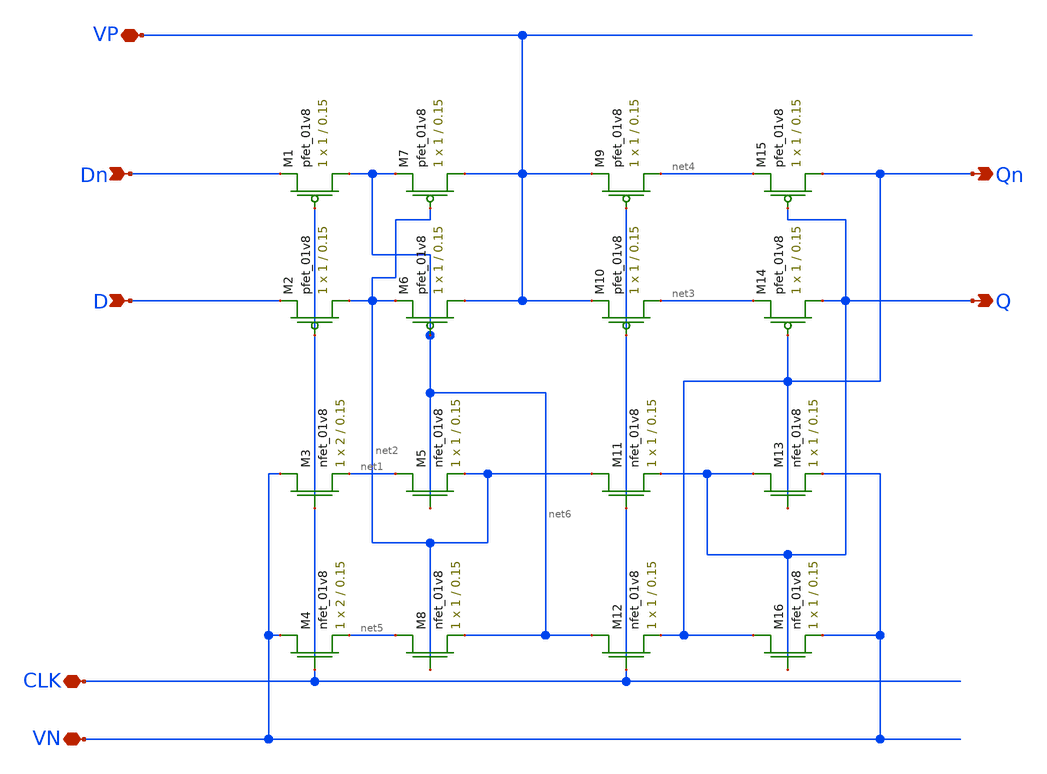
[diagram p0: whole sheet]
** sch_path: MP2/csrl.sch
**.subckt csrl VP VN CLK Dn D Qn Q
*.iopin VP
*.iopin VN
*.iopin CLK
*.ipin Dn
*.ipin D
*.opin Qn
*.opin Q
XM1 net6 CLK Dn VDD sky130_fd_pr__pfet_01v8 L=0.15 W=1 nf=1 ad='int((nf+1)/2) * W/nf * 0.29' as='int((nf+2)/2) * W/nf * 0.29'
+ pd='2*int((nf+1)/2) * (W/nf + 0.29)' ps='2*int((nf+2)/2) * (W/nf + 0.29)' nrd='0.29 / W' nrs='0.29 / W'
+ sa=0 sb=0 sd=0 mult=1 m=1
XM2 net2 CLK D VDD sky130_fd_pr__pfet_01v8 L=0.15 W=1 nf=1 ad='int((nf+1)/2) * W/nf * 0.29' as='int((nf+2)/2) * W/nf * 0.29'
+ pd='2*int((nf+1)/2) * (W/nf + 0.29)' ps='2*int((nf+2)/2) * (W/nf + 0.29)' nrd='0.29 / W' nrs='0.29 / W'
+ sa=0 sb=0 sd=0 mult=1 m=1
XM3 VN CLK net1 GND sky130_fd_pr__nfet_01v8 L=0.15 W=2 nf=1 ad='int((nf+1)/2) * W/nf * 0.29' as='int((nf+2)/2) * W/nf * 0.29'
+ pd='2*int((nf+1)/2) * (W/nf + 0.29)' ps='2*int((nf+2)/2) * (W/nf + 0.29)' nrd='0.29 / W' nrs='0.29 / W'
+ sa=0 sb=0 sd=0 mult=1 m=1
XM4 VN CLK net5 GND sky130_fd_pr__nfet_01v8 L=0.15 W=2 nf=1 ad='int((nf+1)/2) * W/nf * 0.29' as='int((nf+2)/2) * W/nf * 0.29'
+ pd='2*int((nf+1)/2) * (W/nf + 0.29)' ps='2*int((nf+2)/2) * (W/nf + 0.29)' nrd='0.29 / W' nrs='0.29 / W'
+ sa=0 sb=0 sd=0 mult=1 m=1
XM5 net1 net6 net2 GND sky130_fd_pr__nfet_01v8 L=0.15 W=1 nf=1 ad='int((nf+1)/2) * W/nf * 0.29' as='int((nf+2)/2) * W/nf * 0.29'
+ pd='2*int((nf+1)/2) * (W/nf + 0.29)' ps='2*int((nf+2)/2) * (W/nf + 0.29)' nrd='0.29 / W' nrs='0.29 / W'
+ sa=0 sb=0 sd=0 mult=1 m=1
XM6 VP net6 net2 VDD sky130_fd_pr__pfet_01v8 L=0.15 W=1 nf=1 ad='int((nf+1)/2) * W/nf * 0.29' as='int((nf+2)/2) * W/nf * 0.29'
+ pd='2*int((nf+1)/2) * (W/nf + 0.29)' ps='2*int((nf+2)/2) * (W/nf + 0.29)' nrd='0.29 / W' nrs='0.29 / W'
+ sa=0 sb=0 sd=0 mult=1 m=1
XM7 VP net2 net6 VDD sky130_fd_pr__pfet_01v8 L=0.15 W=1 nf=1 ad='int((nf+1)/2) * W/nf * 0.29' as='int((nf+2)/2) * W/nf * 0.29'
+ pd='2*int((nf+1)/2) * (W/nf + 0.29)' ps='2*int((nf+2)/2) * (W/nf + 0.29)' nrd='0.29 / W' nrs='0.29 / W'
+ sa=0 sb=0 sd=0 mult=1 m=1
XM8 net5 net2 net6 GND sky130_fd_pr__nfet_01v8 L=0.15 W=1 nf=1 ad='int((nf+1)/2) * W/nf * 0.29' as='int((nf+2)/2) * W/nf * 0.29'
+ pd='2*int((nf+1)/2) * (W/nf + 0.29)' ps='2*int((nf+2)/2) * (W/nf + 0.29)' nrd='0.29 / W' nrs='0.29 / W'
+ sa=0 sb=0 sd=0 mult=1 m=1
XM9 net4 CLK VP VDD sky130_fd_pr__pfet_01v8 L=0.15 W=1 nf=1 ad='int((nf+1)/2) * W/nf * 0.29' as='int((nf+2)/2) * W/nf * 0.29'
+ pd='2*int((nf+1)/2) * (W/nf + 0.29)' ps='2*int((nf+2)/2) * (W/nf + 0.29)' nrd='0.29 / W' nrs='0.29 / W'
+ sa=0 sb=0 sd=0 mult=1 m=1
XM10 net3 CLK VP VDD sky130_fd_pr__pfet_01v8 L=0.15 W=1 nf=1 ad='int((nf+1)/2) * W/nf * 0.29' as='int((nf+2)/2) * W/nf * 0.29'
+ pd='2*int((nf+1)/2) * (W/nf + 0.29)' ps='2*int((nf+2)/2) * (W/nf + 0.29)' nrd='0.29 / W' nrs='0.29 / W'
+ sa=0 sb=0 sd=0 mult=1 m=1
XM11 net2 CLK Q GND sky130_fd_pr__nfet_01v8 L=0.15 W=1 nf=1 ad='int((nf+1)/2) * W/nf * 0.29' as='int((nf+2)/2) * W/nf * 0.29'
+ pd='2*int((nf+1)/2) * (W/nf + 0.29)' ps='2*int((nf+2)/2) * (W/nf + 0.29)' nrd='0.29 / W' nrs='0.29 / W'
+ sa=0 sb=0 sd=0 mult=1 m=1
XM12 net6 CLK Qn GND sky130_fd_pr__nfet_01v8 L=0.15 W=1 nf=1 ad='int((nf+1)/2) * W/nf * 0.29' as='int((nf+2)/2) * W/nf * 0.29'
+ pd='2*int((nf+1)/2) * (W/nf + 0.29)' ps='2*int((nf+2)/2) * (W/nf + 0.29)' nrd='0.29 / W' nrs='0.29 / W'
+ sa=0 sb=0 sd=0 mult=1 m=1
XM13 Q Qn VN GND sky130_fd_pr__nfet_01v8 L=0.15 W=1 nf=1 ad='int((nf+1)/2) * W/nf * 0.29' as='int((nf+2)/2) * W/nf * 0.29'
+ pd='2*int((nf+1)/2) * (W/nf + 0.29)' ps='2*int((nf+2)/2) * (W/nf + 0.29)' nrd='0.29 / W' nrs='0.29 / W'
+ sa=0 sb=0 sd=0 mult=1 m=1
XM14 Q Qn net3 VDD sky130_fd_pr__pfet_01v8 L=0.15 W=1 nf=1 ad='int((nf+1)/2) * W/nf * 0.29' as='int((nf+2)/2) * W/nf * 0.29'
+ pd='2*int((nf+1)/2) * (W/nf + 0.29)' ps='2*int((nf+2)/2) * (W/nf + 0.29)' nrd='0.29 / W' nrs='0.29 / W'
+ sa=0 sb=0 sd=0 mult=1 m=1
XM15 Qn Q net4 VDD sky130_fd_pr__pfet_01v8 L=0.15 W=1 nf=1 ad='int((nf+1)/2) * W/nf * 0.29' as='int((nf+2)/2) * W/nf * 0.29'
+ pd='2*int((nf+1)/2) * (W/nf + 0.29)' ps='2*int((nf+2)/2) * (W/nf + 0.29)' nrd='0.29 / W' nrs='0.29 / W'
+ sa=0 sb=0 sd=0 mult=1 m=1
XM16 Qn Q VN GND sky130_fd_pr__nfet_01v8 L=0.15 W=1 nf=1 ad='int((nf+1)/2) * W/nf * 0.29' as='int((nf+2)/2) * W/nf * 0.29'
+ pd='2*int((nf+1)/2) * (W/nf + 0.29)' ps='2*int((nf+2)/2) * (W/nf + 0.29)' nrd='0.29 / W' nrs='0.29 / W'
+ sa=0 sb=0 sd=0 mult=1 m=1
**.ends
.end
